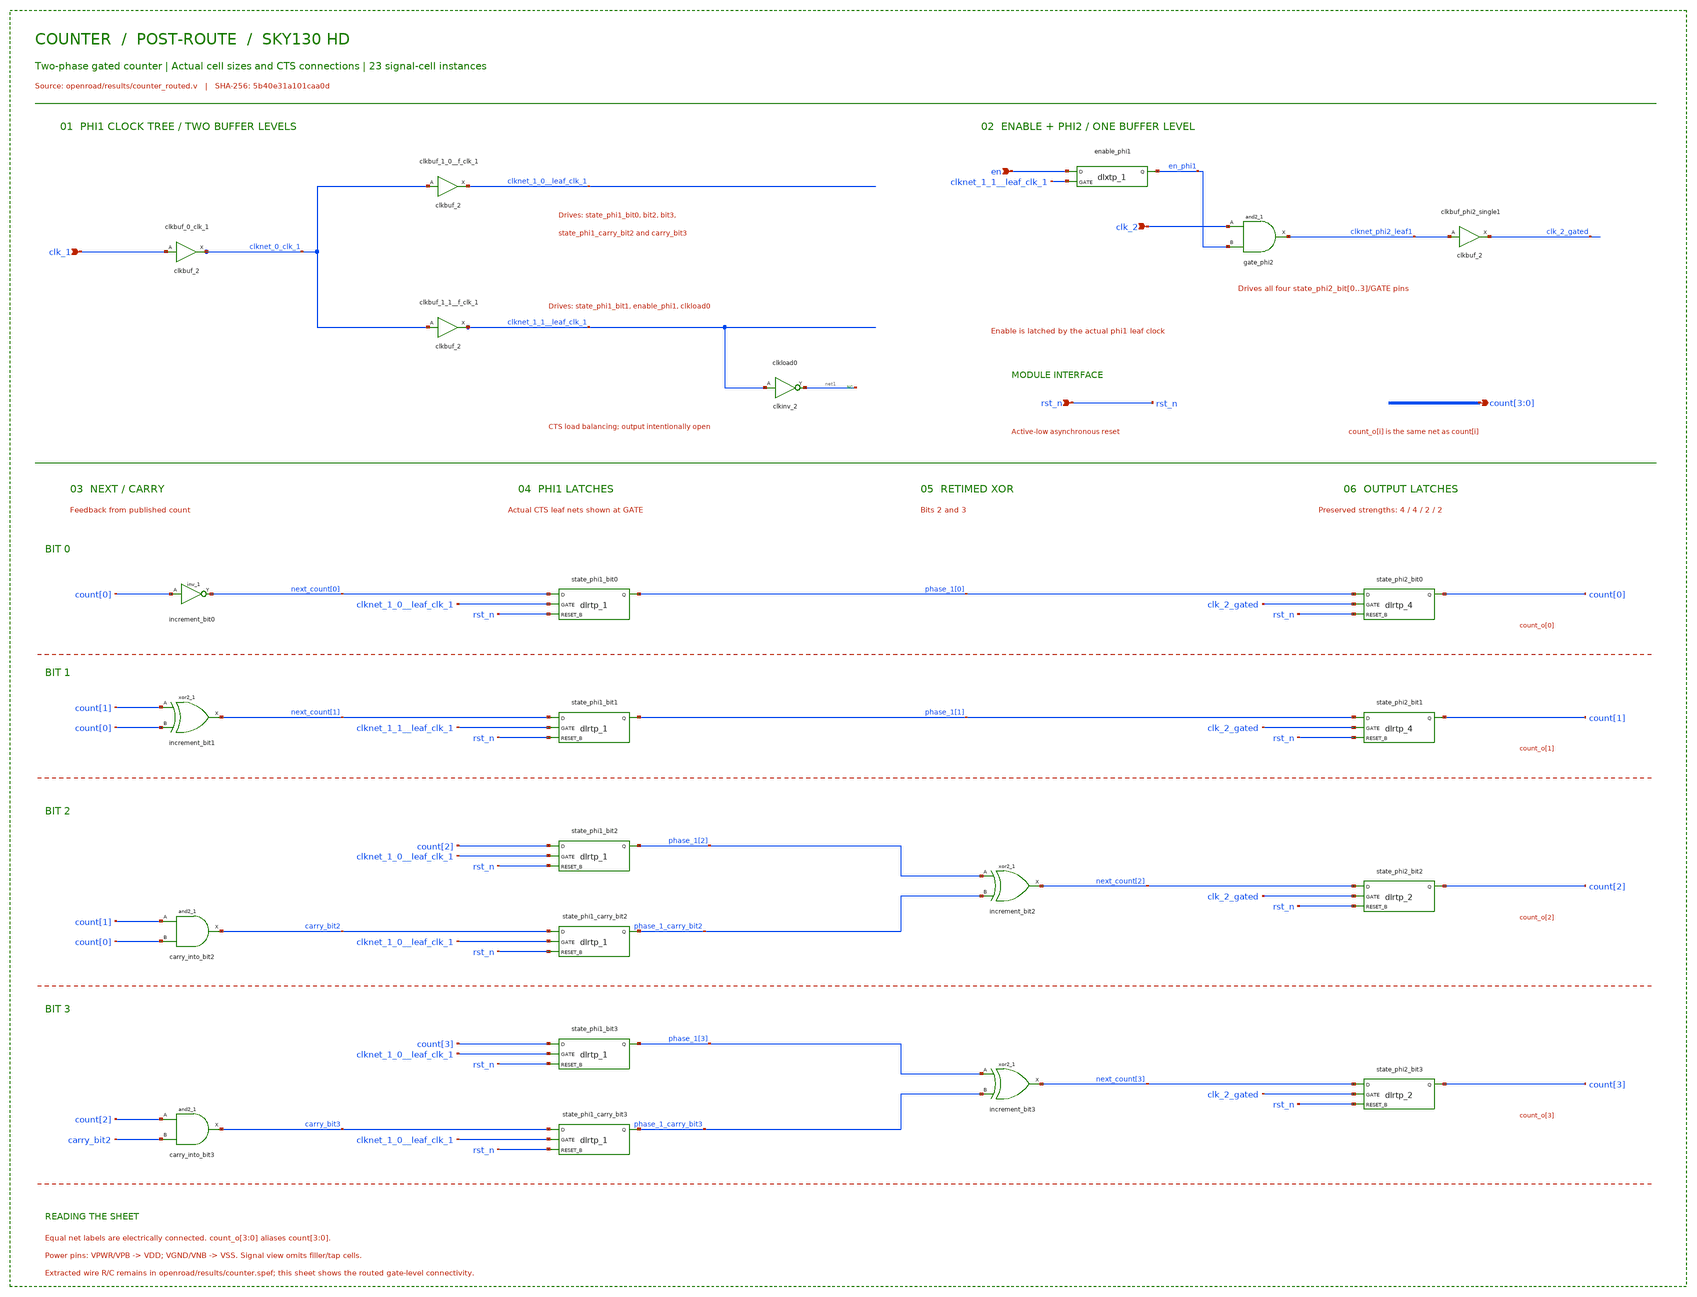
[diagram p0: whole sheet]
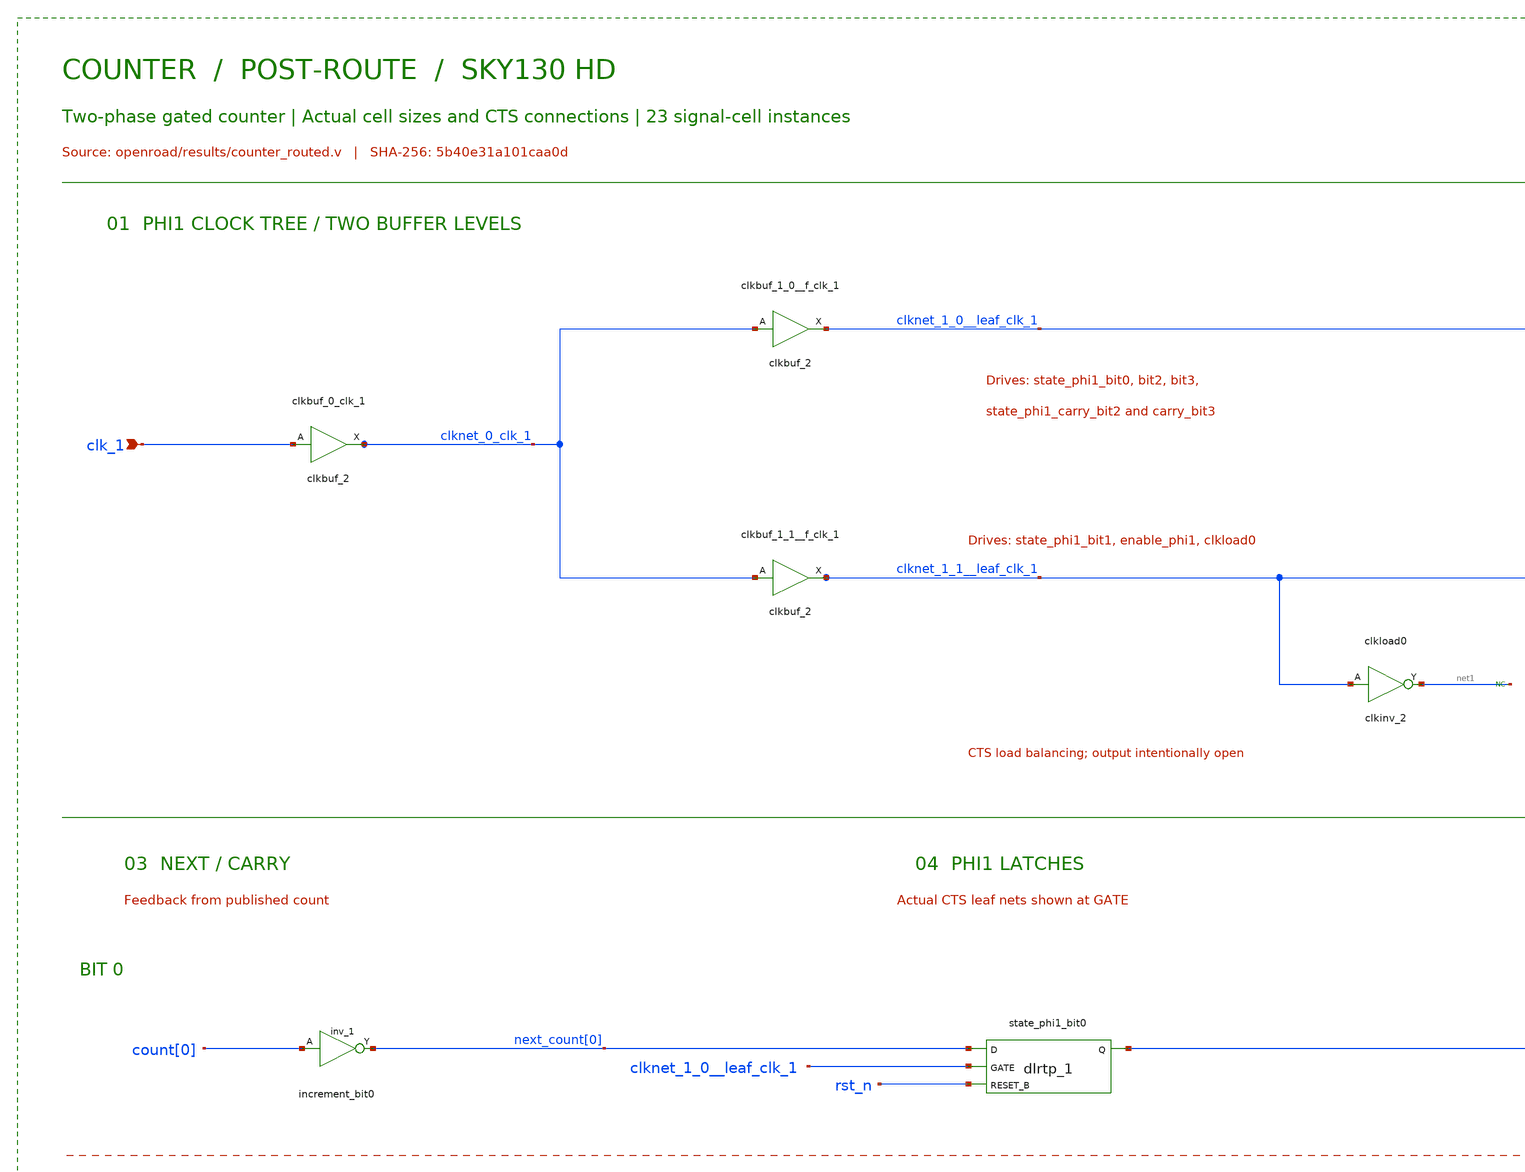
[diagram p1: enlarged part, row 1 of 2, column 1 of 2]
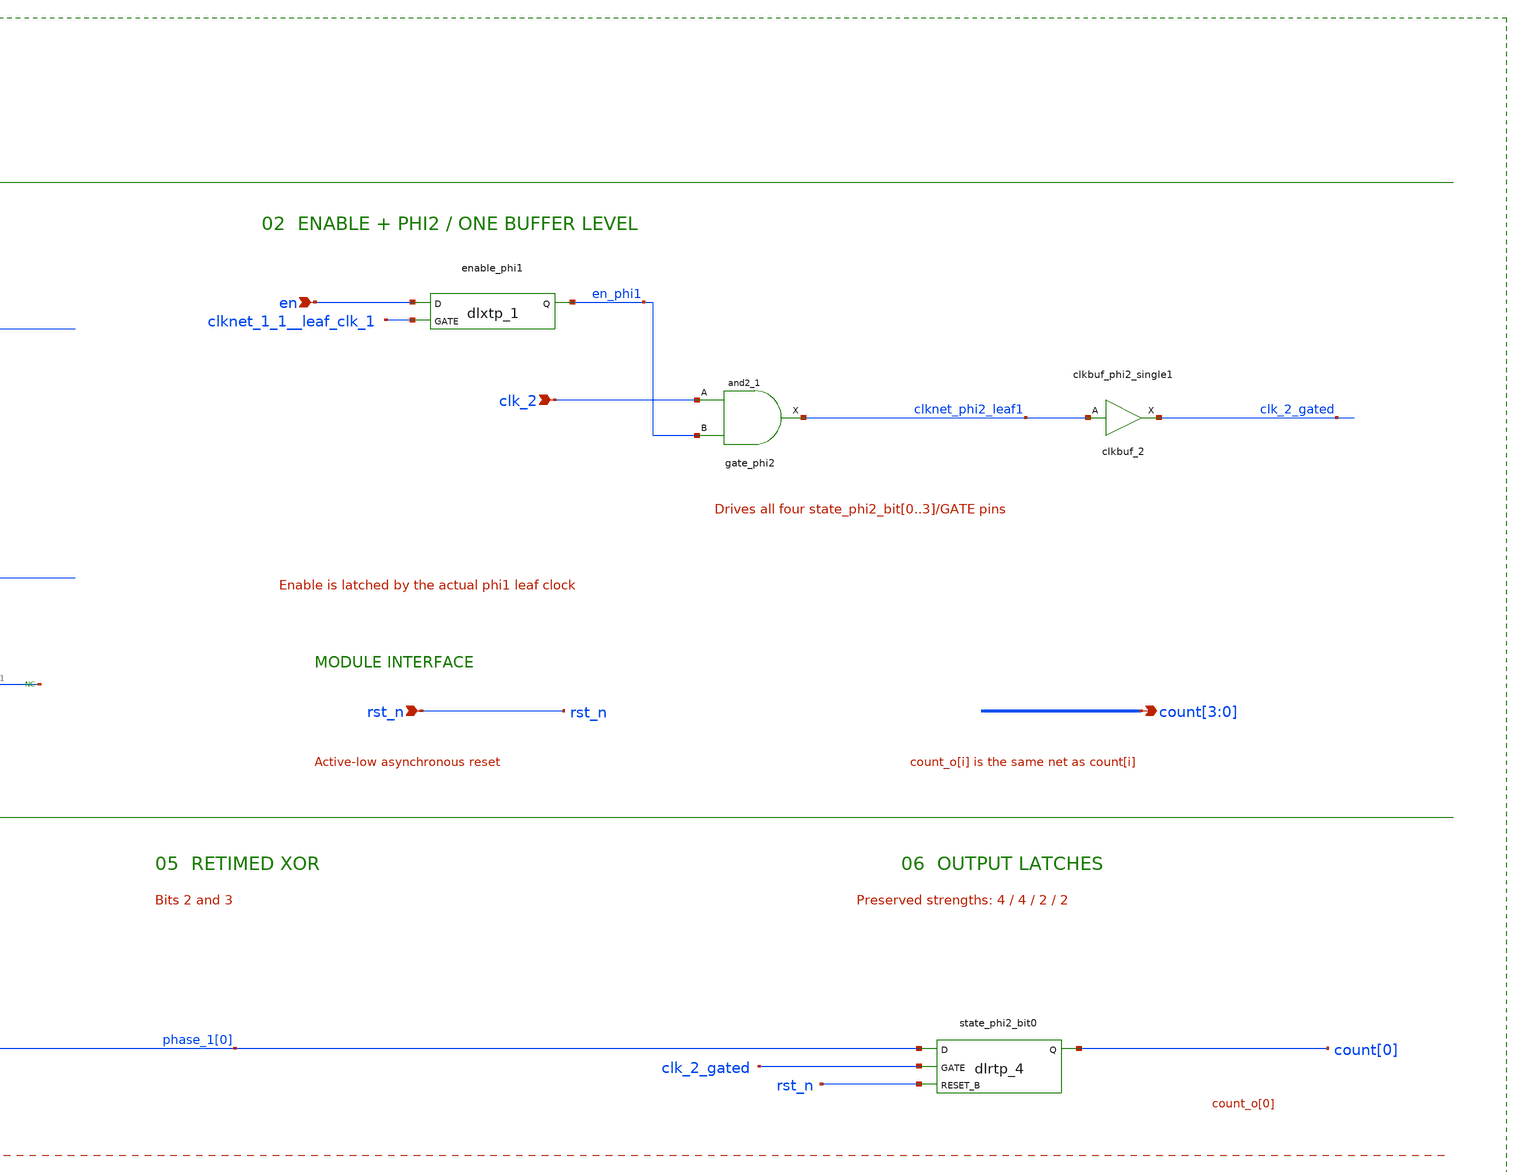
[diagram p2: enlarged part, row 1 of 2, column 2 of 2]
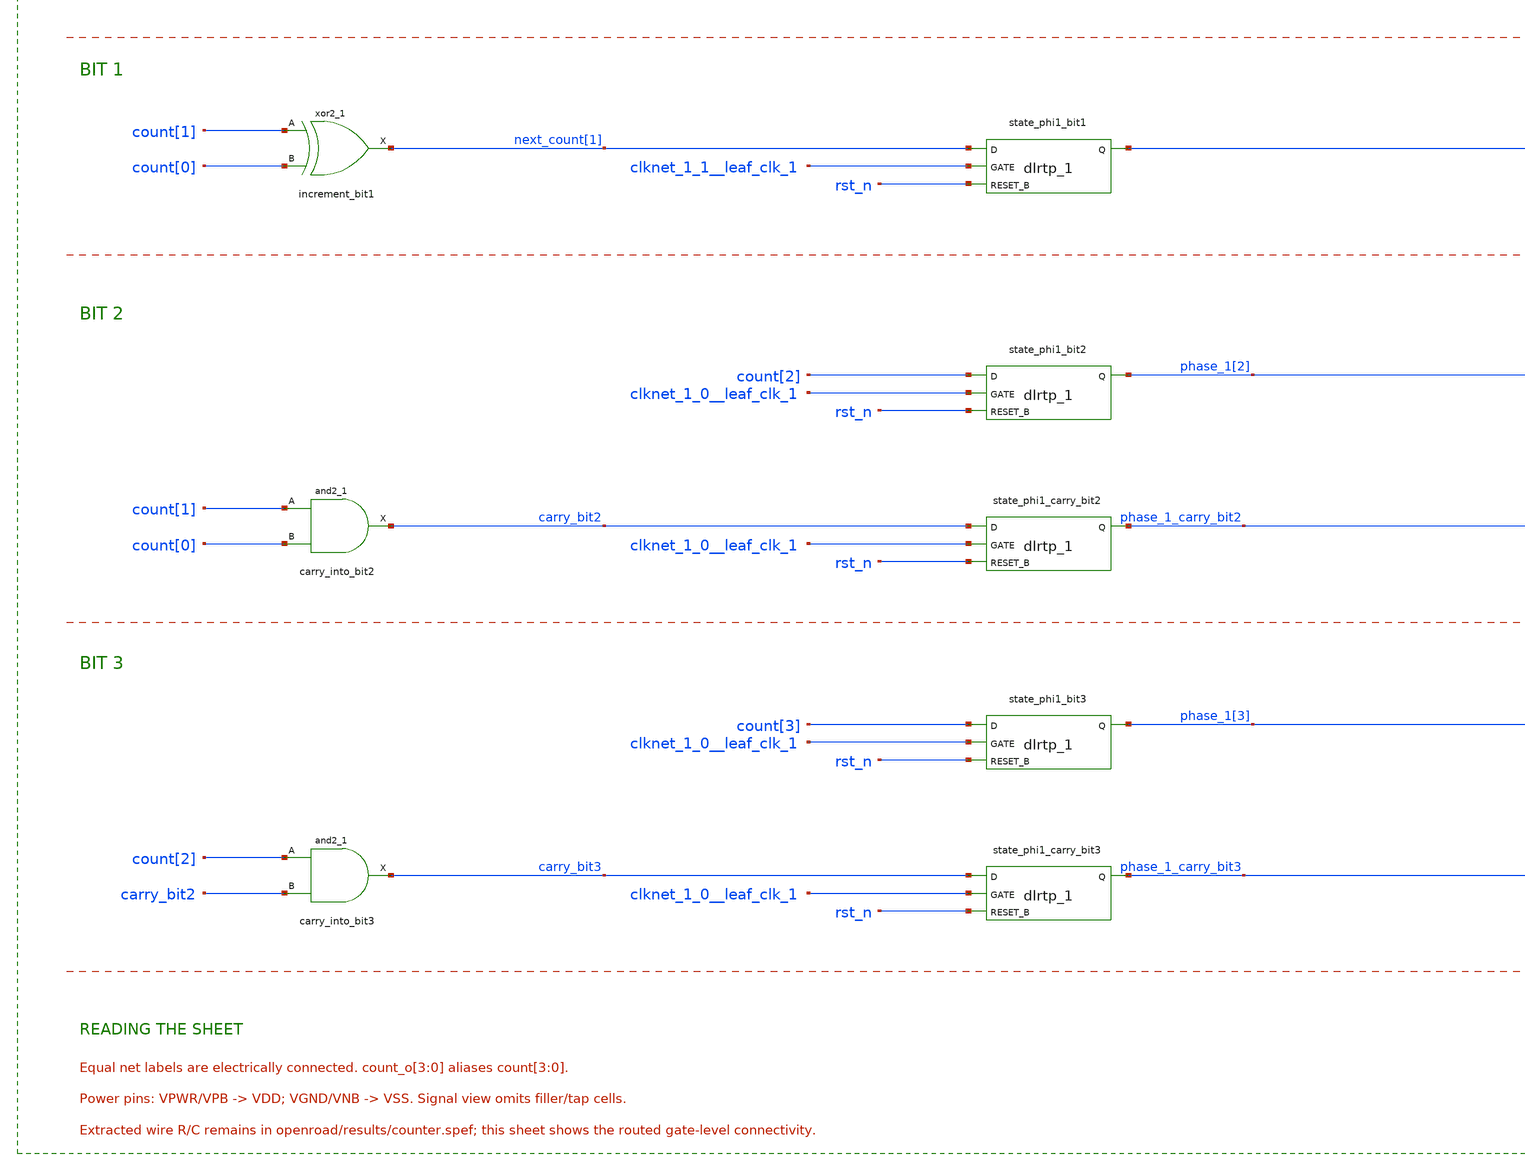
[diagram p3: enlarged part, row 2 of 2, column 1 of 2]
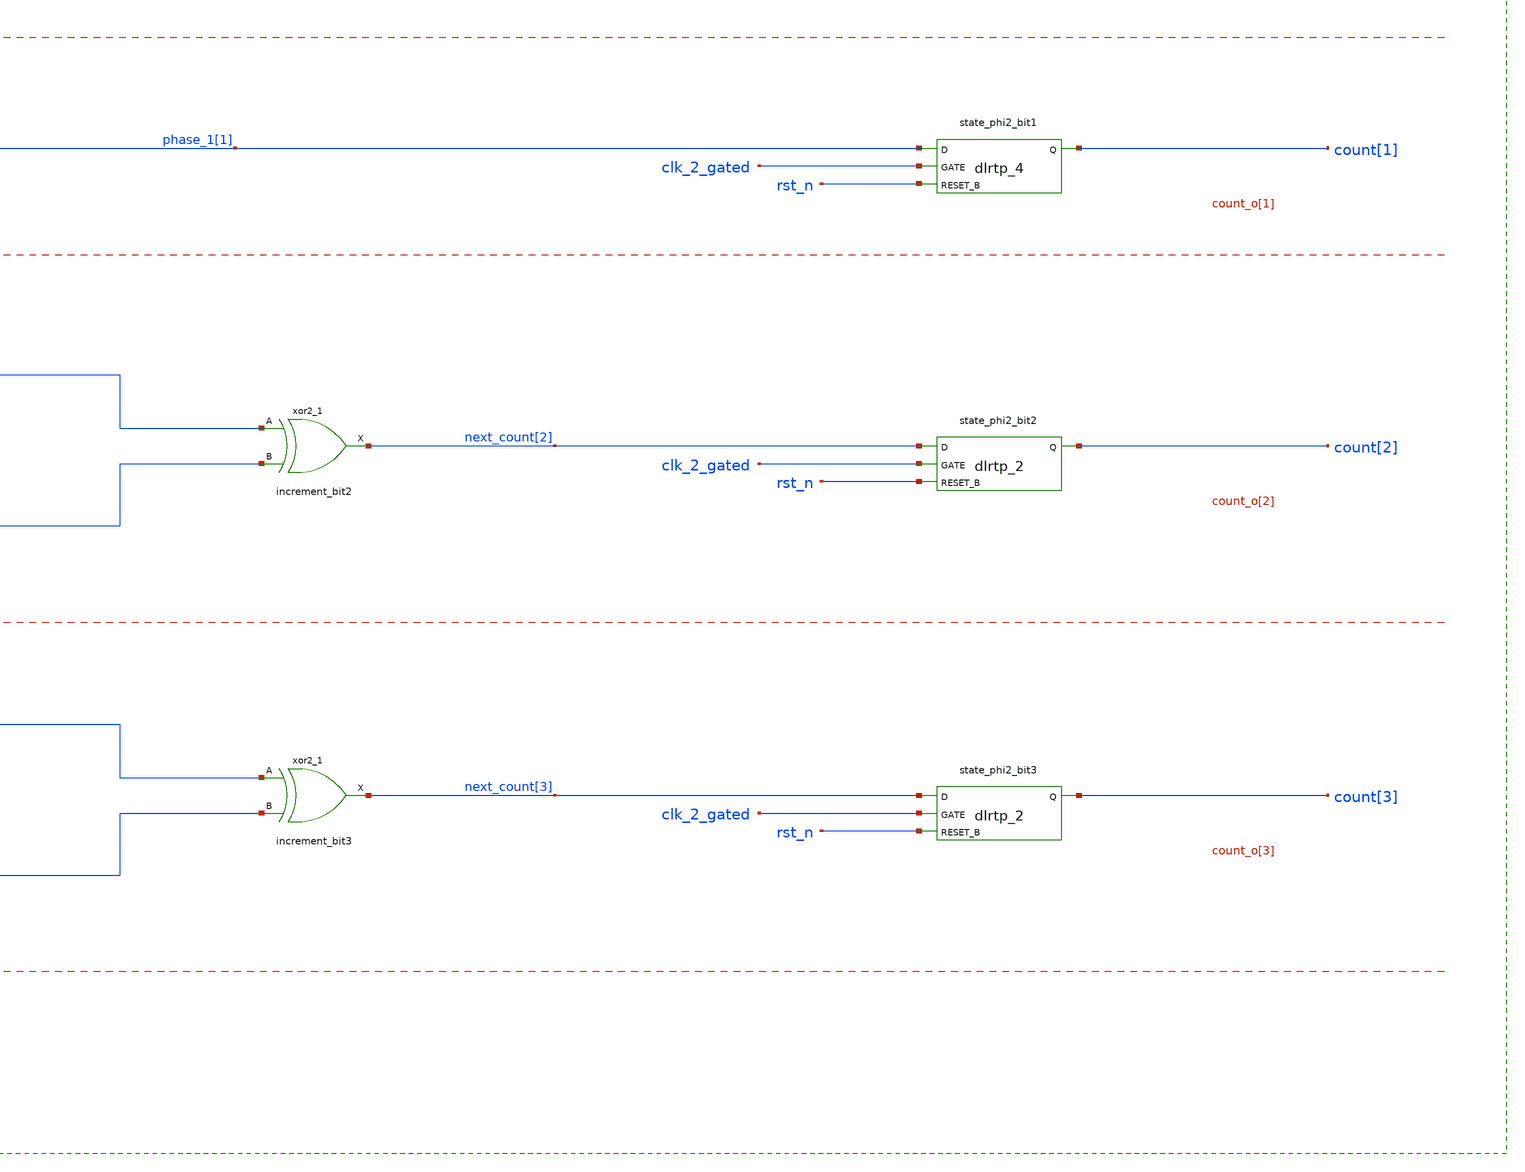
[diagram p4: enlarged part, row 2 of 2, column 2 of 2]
** sch_path: examples/counter/counter_latch_clock/counter_routed.sch
**.subckt counter_routed clk_1 en clk_2 rst_n count[3],count[2],count[1],count[0]
*.ipin clk_1
*.ipin en
*.ipin clk_2
*.ipin rst_n
*.opin count[3],count[2],count[1],count[0]
clkbuf_0_clk_1 clk_1 VSS VSS VDD VDD clknet_0_clk_1 sky130_fd_sc_hd__clkbuf_2
clkbuf_1_0__f_clk_1 clknet_0_clk_1 VSS VSS VDD VDD clknet_1_0__leaf_clk_1 sky130_fd_sc_hd__clkbuf_2
clkbuf_1_1__f_clk_1 clknet_0_clk_1 VSS VSS VDD VDD clknet_1_1__leaf_clk_1 sky130_fd_sc_hd__clkbuf_2
clkload0 clknet_1_1__leaf_clk_1 VSS VSS VDD VDD net1 sky130_fd_sc_hd__clkinv_2
* noconn #net1
enable_phi1 en clknet_1_1__leaf_clk_1 VSS VSS VDD VDD en_phi1 sky130_fd_sc_hd__dlxtp_1
gate_phi2 clk_2 en_phi1 VSS VSS VDD VDD clknet_phi2_leaf1 sky130_fd_sc_hd__and2_1
clkbuf_phi2_single1 clknet_phi2_leaf1 VSS VSS VDD VDD clk_2_gated sky130_fd_sc_hd__clkbuf_2
increment_bit0 count[0] VSS VSS VDD VDD next_count[0] sky130_fd_sc_hd__inv_1
state_phi1_bit0 next_count[0] clknet_1_0__leaf_clk_1 rst_n VSS VSS VDD VDD phase_1[0]
+ sky130_fd_sc_hd__dlrtp_1
state_phi2_bit0 phase_1[0] clk_2_gated rst_n VSS VSS VDD VDD count[0] sky130_fd_sc_hd__dlrtp_4
increment_bit1 count[1] count[0] VSS VSS VDD VDD next_count[1] sky130_fd_sc_hd__xor2_1
state_phi1_bit1 next_count[1] clknet_1_1__leaf_clk_1 rst_n VSS VSS VDD VDD phase_1[1]
+ sky130_fd_sc_hd__dlrtp_1
state_phi2_bit1 phase_1[1] clk_2_gated rst_n VSS VSS VDD VDD count[1] sky130_fd_sc_hd__dlrtp_4
state_phi1_bit2 count[2] clknet_1_0__leaf_clk_1 rst_n VSS VSS VDD VDD phase_1[2]
+ sky130_fd_sc_hd__dlrtp_1
carry_into_bit2 count[1] count[0] VSS VSS VDD VDD carry_bit2 sky130_fd_sc_hd__and2_1
state_phi1_carry_bit2 carry_bit2 clknet_1_0__leaf_clk_1 rst_n VSS VSS VDD VDD phase_1_carry_bit2
+ sky130_fd_sc_hd__dlrtp_1
increment_bit2 phase_1[2] phase_1_carry_bit2 VSS VSS VDD VDD next_count[2] sky130_fd_sc_hd__xor2_1
state_phi2_bit2 next_count[2] clk_2_gated rst_n VSS VSS VDD VDD count[2] sky130_fd_sc_hd__dlrtp_2
state_phi1_bit3 count[3] clknet_1_0__leaf_clk_1 rst_n VSS VSS VDD VDD phase_1[3]
+ sky130_fd_sc_hd__dlrtp_1
carry_into_bit3 count[2] carry_bit2 VSS VSS VDD VDD carry_bit3 sky130_fd_sc_hd__and2_1
state_phi1_carry_bit3 carry_bit3 clknet_1_0__leaf_clk_1 rst_n VSS VSS VDD VDD phase_1_carry_bit3
+ sky130_fd_sc_hd__dlrtp_1
increment_bit3 phase_1[3] phase_1_carry_bit3 VSS VSS VDD VDD next_count[3] sky130_fd_sc_hd__xor2_1
state_phi2_bit3 next_count[3] clk_2_gated rst_n VSS VSS VDD VDD count[3] sky130_fd_sc_hd__dlrtp_2
**.ends
.end
